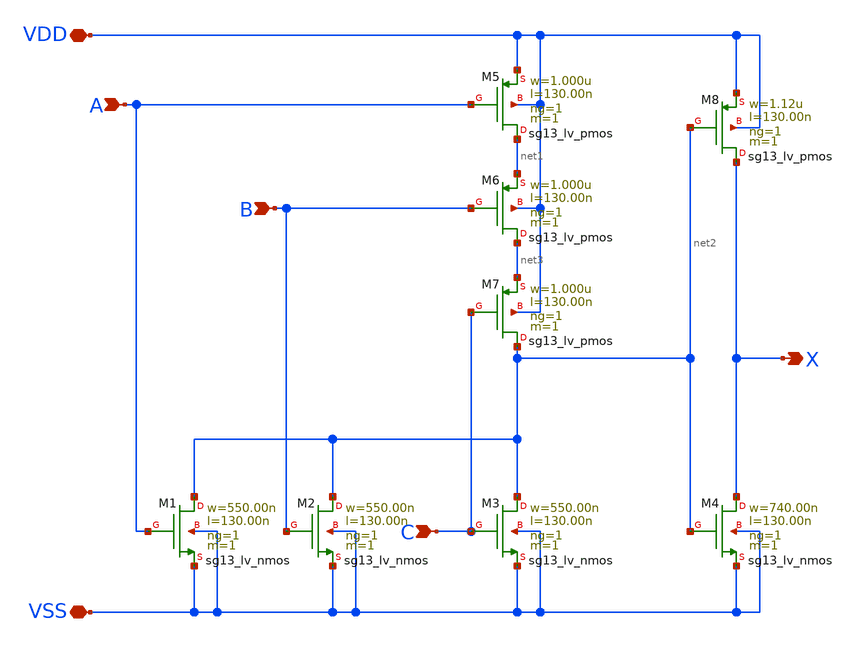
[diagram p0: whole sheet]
** sch_path: ihp-sg13g2/libs.tech/xschem/sg13g2_stdcells/sg13g2_or3_1.sch
* Copyright 2023 IHP PDK Authors
* Licensed under the Apache License, Version 2.0 (the "License");
* you may not use this file except in compliance with the License.
* You may obtain a copy of the License at
* https://www.apache.org/licenses/LICENSE-2.0
* Unless required by applicable law or agreed to in writing, software
* distributed under the License is distributed on an "AS IS" BASIS,
* WITHOUT WARRANTIES OR CONDITIONS OF ANY KIND, either express or implied.
* See the License for the specific language governing permissions and
* limitations under the License.
**.subckt sg13g2_or3_1 X C B A VDD VSS
*.opin X
*.ipin C
*.ipin B
*.ipin A
*.iopin VDD
*.iopin VSS
XM1 net2 A VSS VSS sg13_lv_nmos w=550.00n l=130.00n ng=1 m=1 mm_ok=1
XM2 net2 B VSS VSS sg13_lv_nmos w=550.00n l=130.00n ng=1 m=1 mm_ok=1
XM3 net2 C VSS VSS sg13_lv_nmos w=550.00n l=130.00n ng=1 m=1 mm_ok=1
XM4 X net2 VSS VSS sg13_lv_nmos w=740.00n l=130.00n ng=1 m=1 mm_ok=1
XM5 net1 A VDD VDD sg13_lv_pmos w=1.000u l=130.00n ng=1 m=1 mm_ok=1
XM6 net3 B net1 VDD sg13_lv_pmos w=1.000u l=130.00n ng=1 m=1 mm_ok=1
XM7 net2 C net3 VDD sg13_lv_pmos w=1.000u l=130.00n ng=1 m=1 mm_ok=1
XM8 X net2 VDD VDD sg13_lv_pmos w=1.12u l=130.00n ng=1 m=1 mm_ok=1
**.ends
.end
